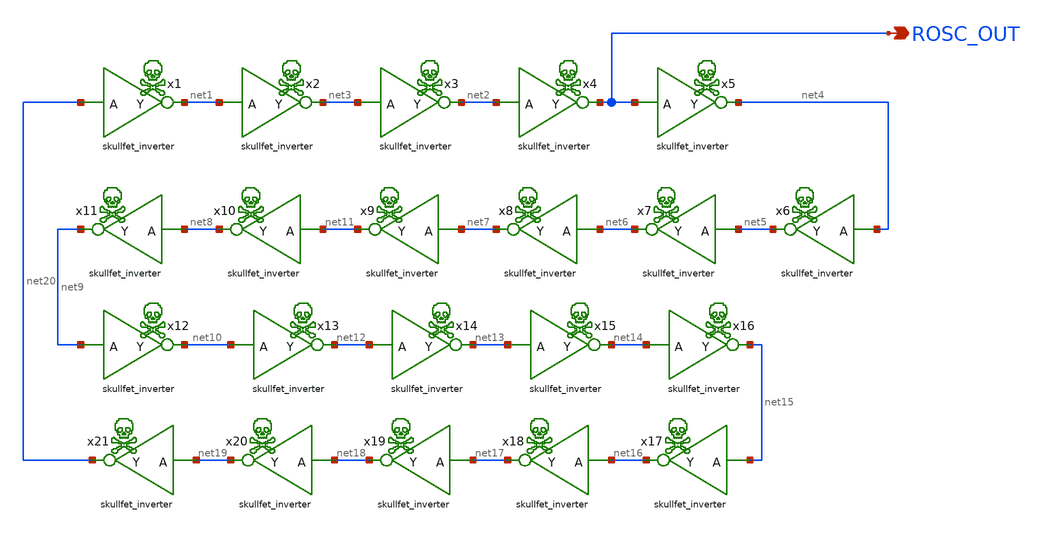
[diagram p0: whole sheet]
** sch_path: xschem/ring.sch
**.subckt ring ROSC_OUT
*.opin ROSC_OUT
x1 net20 net1 skullfet_inverter
x2 net1 net3 skullfet_inverter
x3 net3 net2 skullfet_inverter
x4 net2 ROSC_OUT skullfet_inverter
x5 ROSC_OUT net4 skullfet_inverter
x7 net5 net6 skullfet_inverter
x6 net4 net5 skullfet_inverter
x8 net6 net7 skullfet_inverter
x9 net7 net11 skullfet_inverter
x10 net11 net8 skullfet_inverter
x11 net8 net9 skullfet_inverter
x12 net9 net10 skullfet_inverter
x13 net10 net12 skullfet_inverter
x14 net12 net13 skullfet_inverter
x15 net13 net14 skullfet_inverter
x16 net14 net15 skullfet_inverter
x17 net15 net16 skullfet_inverter
x18 net16 net17 skullfet_inverter
x19 net17 net18 skullfet_inverter
x20 net18 net19 skullfet_inverter
x21 net19 net20 skullfet_inverter
**.ends

* expanding   symbol:  skullfet_inverter.sym # of pins=2
** sym_path: xschem/skullfet_inverter.sym
** sch_path: xschem/skullfet_inverter.sch
.subckt skullfet_inverter A Y
*.ipin A
*.opin Y
XM1 Y A VPWR VPWR sky130_fd_pr__pfet_01v8_hvt L=0.4 W=4.05 nf=1 ad=6.2694 as=4.4307 pd=26.64 ps=10.9
+ nrd='0.29 / 4.05 ' nrs='0.29 / 4.05 ' sa=0 sb=0 sd=0 mult=1 m=1
XM2 Y A VGND VGND sky130_fd_pr__nfet_01v8 L=0.4 W=4.05 nf=1 ad=4.2687 as=6.4314 pd=10.82 ps=26.72 nrd='0.29 / 4.05 '
+ nrs='0.29 / 4.05 ' sa=0 sb=0 sd=0 mult=1 m=1
.ends

.GLOBAL VGND
.GLOBAL VPWR
.end
